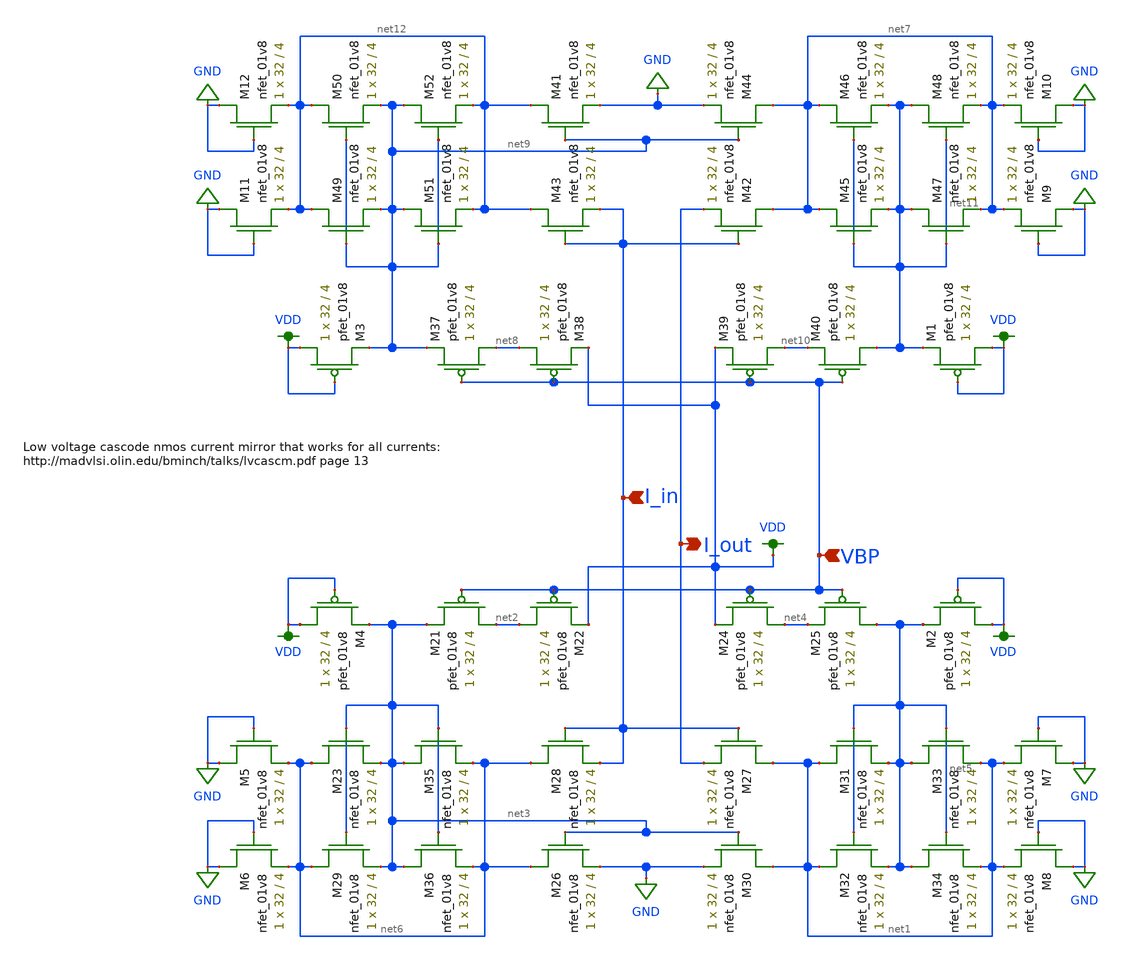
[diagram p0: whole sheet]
** sch_path: schemas/LDS_ALTERNATE_FINAL_CURRENT_MIRROR.sch
**.subckt LDS_ALTERNATE_FINAL_CURRENT_MIRROR I_out VBP I_in
*.opin I_out
*.ipin VBP
*.ipin I_in
XM21 net2 VBP net3 VDD sky130_fd_pr__pfet_01v8 L=4 W=32 nf=1 ad='int((nf+1)/2) * W/nf * 0.29' as='int((nf+2)/2) * W/nf * 0.29'
+ pd='2*int((nf+1)/2) * (W/nf + 0.29)' ps='2*int((nf+2)/2) * (W/nf + 0.29)' nrd='0.29 / W' nrs='0.29 / W'
+ sa=0 sb=0 sd=0 mult=1 m=1
XM22 net2 VBP VDD VDD sky130_fd_pr__pfet_01v8 L=4 W=32 nf=1 ad='int((nf+1)/2) * W/nf * 0.29' as='int((nf+2)/2) * W/nf * 0.29'
+ pd='2*int((nf+1)/2) * (W/nf + 0.29)' ps='2*int((nf+2)/2) * (W/nf + 0.29)' nrd='0.29 / W' nrs='0.29 / W'
+ sa=0 sb=0 sd=0 mult=1 m=1
XM24 net4 VBP VDD VDD sky130_fd_pr__pfet_01v8 L=4 W=32 nf=1 ad='int((nf+1)/2) * W/nf * 0.29' as='int((nf+2)/2) * W/nf * 0.29'
+ pd='2*int((nf+1)/2) * (W/nf + 0.29)' ps='2*int((nf+2)/2) * (W/nf + 0.29)' nrd='0.29 / W' nrs='0.29 / W'
+ sa=0 sb=0 sd=0 mult=1 m=1
XM25 net5 VBP net4 VDD sky130_fd_pr__pfet_01v8 L=4 W=32 nf=1 ad='int((nf+1)/2) * W/nf * 0.29' as='int((nf+2)/2) * W/nf * 0.29'
+ pd='2*int((nf+1)/2) * (W/nf + 0.29)' ps='2*int((nf+2)/2) * (W/nf + 0.29)' nrd='0.29 / W' nrs='0.29 / W'
+ sa=0 sb=0 sd=0 mult=1 m=1
XM26 net6 net3 GND GND sky130_fd_pr__nfet_01v8 L=4 W=32 nf=1 ad='int((nf+1)/2) * W/nf * 0.29' as='int((nf+2)/2) * W/nf * 0.29'
+ pd='2*int((nf+1)/2) * (W/nf + 0.29)' ps='2*int((nf+2)/2) * (W/nf + 0.29)' nrd='0.29 / W' nrs='0.29 / W'
+ sa=0 sb=0 sd=0 mult=1 m=1
XM27 net1 I_in I_out GND sky130_fd_pr__nfet_01v8 L=4 W=32 nf=1 ad='int((nf+1)/2) * W/nf * 0.29' as='int((nf+2)/2) * W/nf * 0.29'
+ pd='2*int((nf+1)/2) * (W/nf + 0.29)' ps='2*int((nf+2)/2) * (W/nf + 0.29)' nrd='0.29 / W' nrs='0.29 / W'
+ sa=0 sb=0 sd=0 mult=1 m=1
XM28 net6 I_in I_in GND sky130_fd_pr__nfet_01v8 L=4 W=32 nf=1 ad='int((nf+1)/2) * W/nf * 0.29' as='int((nf+2)/2) * W/nf * 0.29'
+ pd='2*int((nf+1)/2) * (W/nf + 0.29)' ps='2*int((nf+2)/2) * (W/nf + 0.29)' nrd='0.29 / W' nrs='0.29 / W'
+ sa=0 sb=0 sd=0 mult=1 m=1
XM30 net1 net3 GND GND sky130_fd_pr__nfet_01v8 L=4 W=32 nf=1 ad='int((nf+1)/2) * W/nf * 0.29' as='int((nf+2)/2) * W/nf * 0.29'
+ pd='2*int((nf+1)/2) * (W/nf + 0.29)' ps='2*int((nf+2)/2) * (W/nf + 0.29)' nrd='0.29 / W' nrs='0.29 / W'
+ sa=0 sb=0 sd=0 mult=1 m=1
XM31 net1 net5 net5 GND sky130_fd_pr__nfet_01v8 L=4 W=32 nf=1 ad='int((nf+1)/2) * W/nf * 0.29' as='int((nf+2)/2) * W/nf * 0.29'
+ pd='2*int((nf+1)/2) * (W/nf + 0.29)' ps='2*int((nf+2)/2) * (W/nf + 0.29)' nrd='0.29 / W' nrs='0.29 / W'
+ sa=0 sb=0 sd=0 mult=1 m=1
XM32 net1 net5 net5 GND sky130_fd_pr__nfet_01v8 L=4 W=32 nf=1 ad='int((nf+1)/2) * W/nf * 0.29' as='int((nf+2)/2) * W/nf * 0.29'
+ pd='2*int((nf+1)/2) * (W/nf + 0.29)' ps='2*int((nf+2)/2) * (W/nf + 0.29)' nrd='0.29 / W' nrs='0.29 / W'
+ sa=0 sb=0 sd=0 mult=1 m=1
XM33 net5 net5 net1 GND sky130_fd_pr__nfet_01v8 L=4 W=32 nf=1 ad='int((nf+1)/2) * W/nf * 0.29' as='int((nf+2)/2) * W/nf * 0.29'
+ pd='2*int((nf+1)/2) * (W/nf + 0.29)' ps='2*int((nf+2)/2) * (W/nf + 0.29)' nrd='0.29 / W' nrs='0.29 / W'
+ sa=0 sb=0 sd=0 mult=1 m=1
XM34 net5 net5 net1 GND sky130_fd_pr__nfet_01v8 L=4 W=32 nf=1 ad='int((nf+1)/2) * W/nf * 0.29' as='int((nf+2)/2) * W/nf * 0.29'
+ pd='2*int((nf+1)/2) * (W/nf + 0.29)' ps='2*int((nf+2)/2) * (W/nf + 0.29)' nrd='0.29 / W' nrs='0.29 / W'
+ sa=0 sb=0 sd=0 mult=1 m=1
XM23 net6 net3 net3 GND sky130_fd_pr__nfet_01v8 L=4 W=32 nf=1 ad='int((nf+1)/2) * W/nf * 0.29' as='int((nf+2)/2) * W/nf * 0.29'
+ pd='2*int((nf+1)/2) * (W/nf + 0.29)' ps='2*int((nf+2)/2) * (W/nf + 0.29)' nrd='0.29 / W' nrs='0.29 / W'
+ sa=0 sb=0 sd=0 mult=1 m=1
XM29 net6 net3 net3 GND sky130_fd_pr__nfet_01v8 L=4 W=32 nf=1 ad='int((nf+1)/2) * W/nf * 0.29' as='int((nf+2)/2) * W/nf * 0.29'
+ pd='2*int((nf+1)/2) * (W/nf + 0.29)' ps='2*int((nf+2)/2) * (W/nf + 0.29)' nrd='0.29 / W' nrs='0.29 / W'
+ sa=0 sb=0 sd=0 mult=1 m=1
XM35 net3 net3 net6 GND sky130_fd_pr__nfet_01v8 L=4 W=32 nf=1 ad='int((nf+1)/2) * W/nf * 0.29' as='int((nf+2)/2) * W/nf * 0.29'
+ pd='2*int((nf+1)/2) * (W/nf + 0.29)' ps='2*int((nf+2)/2) * (W/nf + 0.29)' nrd='0.29 / W' nrs='0.29 / W'
+ sa=0 sb=0 sd=0 mult=1 m=1
XM36 net3 net3 net6 GND sky130_fd_pr__nfet_01v8 L=4 W=32 nf=1 ad='int((nf+1)/2) * W/nf * 0.29' as='int((nf+2)/2) * W/nf * 0.29'
+ pd='2*int((nf+1)/2) * (W/nf + 0.29)' ps='2*int((nf+2)/2) * (W/nf + 0.29)' nrd='0.29 / W' nrs='0.29 / W'
+ sa=0 sb=0 sd=0 mult=1 m=1
XM37 net8 VBP net9 VDD sky130_fd_pr__pfet_01v8 L=4 W=32 nf=1 ad='int((nf+1)/2) * W/nf * 0.29' as='int((nf+2)/2) * W/nf * 0.29'
+ pd='2*int((nf+1)/2) * (W/nf + 0.29)' ps='2*int((nf+2)/2) * (W/nf + 0.29)' nrd='0.29 / W' nrs='0.29 / W'
+ sa=0 sb=0 sd=0 mult=1 m=1
XM38 net8 VBP VDD VDD sky130_fd_pr__pfet_01v8 L=4 W=32 nf=1 ad='int((nf+1)/2) * W/nf * 0.29' as='int((nf+2)/2) * W/nf * 0.29'
+ pd='2*int((nf+1)/2) * (W/nf + 0.29)' ps='2*int((nf+2)/2) * (W/nf + 0.29)' nrd='0.29 / W' nrs='0.29 / W'
+ sa=0 sb=0 sd=0 mult=1 m=1
XM39 net10 VBP VDD VDD sky130_fd_pr__pfet_01v8 L=4 W=32 nf=1 ad='int((nf+1)/2) * W/nf * 0.29' as='int((nf+2)/2) * W/nf * 0.29'
+ pd='2*int((nf+1)/2) * (W/nf + 0.29)' ps='2*int((nf+2)/2) * (W/nf + 0.29)' nrd='0.29 / W' nrs='0.29 / W'
+ sa=0 sb=0 sd=0 mult=1 m=1
XM40 net11 VBP net10 VDD sky130_fd_pr__pfet_01v8 L=4 W=32 nf=1 ad='int((nf+1)/2) * W/nf * 0.29' as='int((nf+2)/2) * W/nf * 0.29'
+ pd='2*int((nf+1)/2) * (W/nf + 0.29)' ps='2*int((nf+2)/2) * (W/nf + 0.29)' nrd='0.29 / W' nrs='0.29 / W'
+ sa=0 sb=0 sd=0 mult=1 m=1
XM41 net12 net9 GND GND sky130_fd_pr__nfet_01v8 L=4 W=32 nf=1 ad='int((nf+1)/2) * W/nf * 0.29' as='int((nf+2)/2) * W/nf * 0.29'
+ pd='2*int((nf+1)/2) * (W/nf + 0.29)' ps='2*int((nf+2)/2) * (W/nf + 0.29)' nrd='0.29 / W' nrs='0.29 / W'
+ sa=0 sb=0 sd=0 mult=1 m=1
XM42 net7 I_in I_out GND sky130_fd_pr__nfet_01v8 L=4 W=32 nf=1 ad='int((nf+1)/2) * W/nf * 0.29' as='int((nf+2)/2) * W/nf * 0.29'
+ pd='2*int((nf+1)/2) * (W/nf + 0.29)' ps='2*int((nf+2)/2) * (W/nf + 0.29)' nrd='0.29 / W' nrs='0.29 / W'
+ sa=0 sb=0 sd=0 mult=1 m=1
XM43 net12 I_in I_in GND sky130_fd_pr__nfet_01v8 L=4 W=32 nf=1 ad='int((nf+1)/2) * W/nf * 0.29' as='int((nf+2)/2) * W/nf * 0.29'
+ pd='2*int((nf+1)/2) * (W/nf + 0.29)' ps='2*int((nf+2)/2) * (W/nf + 0.29)' nrd='0.29 / W' nrs='0.29 / W'
+ sa=0 sb=0 sd=0 mult=1 m=1
XM44 net7 net9 GND GND sky130_fd_pr__nfet_01v8 L=4 W=32 nf=1 ad='int((nf+1)/2) * W/nf * 0.29' as='int((nf+2)/2) * W/nf * 0.29'
+ pd='2*int((nf+1)/2) * (W/nf + 0.29)' ps='2*int((nf+2)/2) * (W/nf + 0.29)' nrd='0.29 / W' nrs='0.29 / W'
+ sa=0 sb=0 sd=0 mult=1 m=1
XM45 net7 net11 net11 GND sky130_fd_pr__nfet_01v8 L=4 W=32 nf=1 ad='int((nf+1)/2) * W/nf * 0.29' as='int((nf+2)/2) * W/nf * 0.29'
+ pd='2*int((nf+1)/2) * (W/nf + 0.29)' ps='2*int((nf+2)/2) * (W/nf + 0.29)' nrd='0.29 / W' nrs='0.29 / W'
+ sa=0 sb=0 sd=0 mult=1 m=1
XM46 net7 net11 net11 GND sky130_fd_pr__nfet_01v8 L=4 W=32 nf=1 ad='int((nf+1)/2) * W/nf * 0.29' as='int((nf+2)/2) * W/nf * 0.29'
+ pd='2*int((nf+1)/2) * (W/nf + 0.29)' ps='2*int((nf+2)/2) * (W/nf + 0.29)' nrd='0.29 / W' nrs='0.29 / W'
+ sa=0 sb=0 sd=0 mult=1 m=1
XM47 net11 net11 net7 GND sky130_fd_pr__nfet_01v8 L=4 W=32 nf=1 ad='int((nf+1)/2) * W/nf * 0.29' as='int((nf+2)/2) * W/nf * 0.29'
+ pd='2*int((nf+1)/2) * (W/nf + 0.29)' ps='2*int((nf+2)/2) * (W/nf + 0.29)' nrd='0.29 / W' nrs='0.29 / W'
+ sa=0 sb=0 sd=0 mult=1 m=1
XM48 net11 net11 net7 GND sky130_fd_pr__nfet_01v8 L=4 W=32 nf=1 ad='int((nf+1)/2) * W/nf * 0.29' as='int((nf+2)/2) * W/nf * 0.29'
+ pd='2*int((nf+1)/2) * (W/nf + 0.29)' ps='2*int((nf+2)/2) * (W/nf + 0.29)' nrd='0.29 / W' nrs='0.29 / W'
+ sa=0 sb=0 sd=0 mult=1 m=1
XM49 net12 net9 net9 GND sky130_fd_pr__nfet_01v8 L=4 W=32 nf=1 ad='int((nf+1)/2) * W/nf * 0.29' as='int((nf+2)/2) * W/nf * 0.29'
+ pd='2*int((nf+1)/2) * (W/nf + 0.29)' ps='2*int((nf+2)/2) * (W/nf + 0.29)' nrd='0.29 / W' nrs='0.29 / W'
+ sa=0 sb=0 sd=0 mult=1 m=1
XM50 net12 net9 net9 GND sky130_fd_pr__nfet_01v8 L=4 W=32 nf=1 ad='int((nf+1)/2) * W/nf * 0.29' as='int((nf+2)/2) * W/nf * 0.29'
+ pd='2*int((nf+1)/2) * (W/nf + 0.29)' ps='2*int((nf+2)/2) * (W/nf + 0.29)' nrd='0.29 / W' nrs='0.29 / W'
+ sa=0 sb=0 sd=0 mult=1 m=1
XM51 net9 net9 net12 GND sky130_fd_pr__nfet_01v8 L=4 W=32 nf=1 ad='int((nf+1)/2) * W/nf * 0.29' as='int((nf+2)/2) * W/nf * 0.29'
+ pd='2*int((nf+1)/2) * (W/nf + 0.29)' ps='2*int((nf+2)/2) * (W/nf + 0.29)' nrd='0.29 / W' nrs='0.29 / W'
+ sa=0 sb=0 sd=0 mult=1 m=1
XM52 net9 net9 net12 GND sky130_fd_pr__nfet_01v8 L=4 W=32 nf=1 ad='int((nf+1)/2) * W/nf * 0.29' as='int((nf+2)/2) * W/nf * 0.29'
+ pd='2*int((nf+1)/2) * (W/nf + 0.29)' ps='2*int((nf+2)/2) * (W/nf + 0.29)' nrd='0.29 / W' nrs='0.29 / W'
+ sa=0 sb=0 sd=0 mult=1 m=1
XM1 VDD VDD net11 VDD sky130_fd_pr__pfet_01v8 L=4 W=32 nf=1 ad='int((nf+1)/2) * W/nf * 0.29' as='int((nf+2)/2) * W/nf * 0.29'
+ pd='2*int((nf+1)/2) * (W/nf + 0.29)' ps='2*int((nf+2)/2) * (W/nf + 0.29)' nrd='0.29 / W' nrs='0.29 / W'
+ sa=0 sb=0 sd=0 mult=1 m=1
XM2 VDD VDD net5 VDD sky130_fd_pr__pfet_01v8 L=4 W=32 nf=1 ad='int((nf+1)/2) * W/nf * 0.29' as='int((nf+2)/2) * W/nf * 0.29'
+ pd='2*int((nf+1)/2) * (W/nf + 0.29)' ps='2*int((nf+2)/2) * (W/nf + 0.29)' nrd='0.29 / W' nrs='0.29 / W'
+ sa=0 sb=0 sd=0 mult=1 m=1
XM3 VDD VDD net9 VDD sky130_fd_pr__pfet_01v8 L=4 W=32 nf=1 ad='int((nf+1)/2) * W/nf * 0.29' as='int((nf+2)/2) * W/nf * 0.29'
+ pd='2*int((nf+1)/2) * (W/nf + 0.29)' ps='2*int((nf+2)/2) * (W/nf + 0.29)' nrd='0.29 / W' nrs='0.29 / W'
+ sa=0 sb=0 sd=0 mult=1 m=1
XM4 VDD VDD net3 VDD sky130_fd_pr__pfet_01v8 L=4 W=32 nf=1 ad='int((nf+1)/2) * W/nf * 0.29' as='int((nf+2)/2) * W/nf * 0.29'
+ pd='2*int((nf+1)/2) * (W/nf + 0.29)' ps='2*int((nf+2)/2) * (W/nf + 0.29)' nrd='0.29 / W' nrs='0.29 / W'
+ sa=0 sb=0 sd=0 mult=1 m=1
XM5 GND GND net6 GND sky130_fd_pr__nfet_01v8 L=4 W=32 nf=1 ad='int((nf+1)/2) * W/nf * 0.29' as='int((nf+2)/2) * W/nf * 0.29'
+ pd='2*int((nf+1)/2) * (W/nf + 0.29)' ps='2*int((nf+2)/2) * (W/nf + 0.29)' nrd='0.29 / W' nrs='0.29 / W'
+ sa=0 sb=0 sd=0 mult=1 m=1
XM6 GND GND net6 GND sky130_fd_pr__nfet_01v8 L=4 W=32 nf=1 ad='int((nf+1)/2) * W/nf * 0.29' as='int((nf+2)/2) * W/nf * 0.29'
+ pd='2*int((nf+1)/2) * (W/nf + 0.29)' ps='2*int((nf+2)/2) * (W/nf + 0.29)' nrd='0.29 / W' nrs='0.29 / W'
+ sa=0 sb=0 sd=0 mult=1 m=1
XM7 GND GND net1 GND sky130_fd_pr__nfet_01v8 L=4 W=32 nf=1 ad='int((nf+1)/2) * W/nf * 0.29' as='int((nf+2)/2) * W/nf * 0.29'
+ pd='2*int((nf+1)/2) * (W/nf + 0.29)' ps='2*int((nf+2)/2) * (W/nf + 0.29)' nrd='0.29 / W' nrs='0.29 / W'
+ sa=0 sb=0 sd=0 mult=1 m=1
XM8 GND GND net1 GND sky130_fd_pr__nfet_01v8 L=4 W=32 nf=1 ad='int((nf+1)/2) * W/nf * 0.29' as='int((nf+2)/2) * W/nf * 0.29'
+ pd='2*int((nf+1)/2) * (W/nf + 0.29)' ps='2*int((nf+2)/2) * (W/nf + 0.29)' nrd='0.29 / W' nrs='0.29 / W'
+ sa=0 sb=0 sd=0 mult=1 m=1
XM9 GND GND net7 GND sky130_fd_pr__nfet_01v8 L=4 W=32 nf=1 ad='int((nf+1)/2) * W/nf * 0.29' as='int((nf+2)/2) * W/nf * 0.29'
+ pd='2*int((nf+1)/2) * (W/nf + 0.29)' ps='2*int((nf+2)/2) * (W/nf + 0.29)' nrd='0.29 / W' nrs='0.29 / W'
+ sa=0 sb=0 sd=0 mult=1 m=1
XM10 GND GND net7 GND sky130_fd_pr__nfet_01v8 L=4 W=32 nf=1 ad='int((nf+1)/2) * W/nf * 0.29' as='int((nf+2)/2) * W/nf * 0.29'
+ pd='2*int((nf+1)/2) * (W/nf + 0.29)' ps='2*int((nf+2)/2) * (W/nf + 0.29)' nrd='0.29 / W' nrs='0.29 / W'
+ sa=0 sb=0 sd=0 mult=1 m=1
XM11 GND GND net12 GND sky130_fd_pr__nfet_01v8 L=4 W=32 nf=1 ad='int((nf+1)/2) * W/nf * 0.29' as='int((nf+2)/2) * W/nf * 0.29'
+ pd='2*int((nf+1)/2) * (W/nf + 0.29)' ps='2*int((nf+2)/2) * (W/nf + 0.29)' nrd='0.29 / W' nrs='0.29 / W'
+ sa=0 sb=0 sd=0 mult=1 m=1
XM12 GND GND net12 GND sky130_fd_pr__nfet_01v8 L=4 W=32 nf=1 ad='int((nf+1)/2) * W/nf * 0.29' as='int((nf+2)/2) * W/nf * 0.29'
+ pd='2*int((nf+1)/2) * (W/nf + 0.29)' ps='2*int((nf+2)/2) * (W/nf + 0.29)' nrd='0.29 / W' nrs='0.29 / W'
+ sa=0 sb=0 sd=0 mult=1 m=1
**.ends
.GLOBAL GND
.GLOBAL VDD
.end
